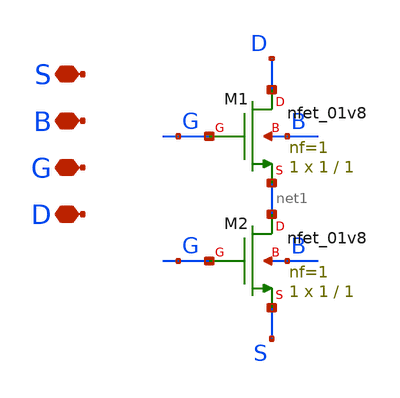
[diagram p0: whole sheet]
** sch_path: xschem/INA_layout_v2/bias/nfet_2series.sch
**.subckt nfet_2series S B G D
*.iopin S
*.iopin B
*.iopin G
*.iopin D
XM1 D G net1 B sky130_fd_pr__nfet_01v8 L=1 W=1 nf=1 ad='int((nf+1)/2) * W/nf * 0.29' as='int((nf+2)/2) * W/nf * 0.29'
+ pd='2*int((nf+1)/2) * (W/nf + 0.29)' ps='2*int((nf+2)/2) * (W/nf + 0.29)' nrd='0.29 / W' nrs='0.29 / W'
+ sa=0 sb=0 sd=0 mult=1 m=1
XM2 net1 G S B sky130_fd_pr__nfet_01v8 L=1 W=1 nf=1 ad='int((nf+1)/2) * W/nf * 0.29' as='int((nf+2)/2) * W/nf * 0.29'
+ pd='2*int((nf+1)/2) * (W/nf + 0.29)' ps='2*int((nf+2)/2) * (W/nf + 0.29)' nrd='0.29 / W' nrs='0.29 / W'
+ sa=0 sb=0 sd=0 mult=1 m=1
**.ends
.end
